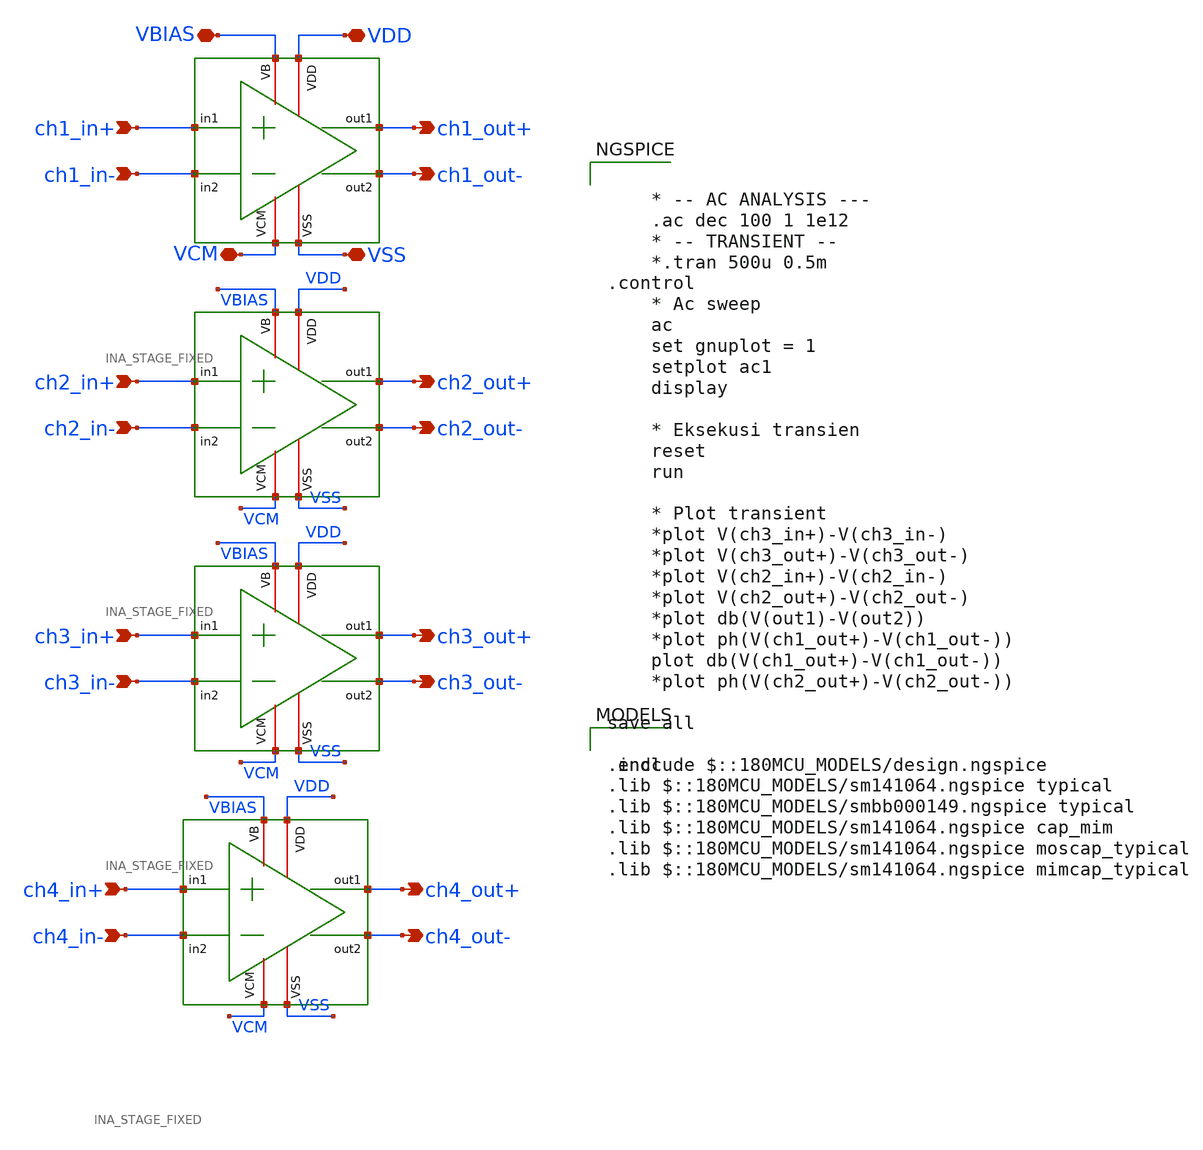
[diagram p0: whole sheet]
** sch_path: ISSCC26/submitted_notebooks/Low Mismatch 4 Channels Instrumentation Amplifier/Instrumentation Amplifier/Schematic and Testbench/FULL_INA_TB.sch
**.subckt FULL_INA_TB ch1_out- ch1_out+ ch1_in+ ch1_in- VCM VBIAS VDD ch2_out- ch2_in+ ch2_in-
*+ ch3_out+ ch3_in+ ch3_in- ch4_out- ch4_out+ ch4_in+ ch4_in- VSS ch3_out- ch2_out+
*.opin ch1_out-
*.opin ch1_out+
*.ipin ch1_in+
*.ipin ch1_in-
*.iopin VCM
*.iopin VBIAS
*.iopin VDD
*.opin ch2_out-
*.ipin ch2_in+
*.ipin ch2_in-
*.opin ch3_out+
*.ipin ch3_in+
*.ipin ch3_in-
*.opin ch4_out-
*.opin ch4_out+
*.ipin ch4_in+
*.ipin ch4_in-
*.iopin VSS
*.opin ch3_out-
*.opin ch2_out+
x1 VCM VDD VBIAS ch1_out- ch1_out+ ch1_in+ ch1_in- VSS INA_STAGE_FIXED
x2 VCM VDD VBIAS ch2_out- ch2_out+ ch2_in+ ch2_in- VSS INA_STAGE_FIXED
x3 VCM VDD VBIAS ch3_out- ch3_out+ ch3_in+ ch3_in- VSS INA_STAGE_FIXED
x4 VCM VDD VBIAS ch4_out- ch4_out+ ch4_in+ ch4_in- VSS INA_STAGE_FIXED
**** begin user architecture code

.include $::180MCU_MODELS/design.ngspice
.lib $::180MCU_MODELS/sm141064.ngspice typical
.lib $::180MCU_MODELS/smbb000149.ngspice typical
.lib $::180MCU_MODELS/sm141064.ngspice cap_mim
.lib $::180MCU_MODELS/sm141064.ngspice moscap_typical
.lib $::180MCU_MODELS/sm141064.ngspice mimcap_typical



	* -- AC ANALYSIS ---
	.ac dec 100 1 1e12
	* -- TRANSIENT --
	*.tran 500u 0.5m
.control
	* Ac sweep
	ac
	set gnuplot = 1
	setplot ac1
	display

	* Eksekusi transien
	reset
	run

	* Plot transient
	*plot V(ch3_in+)-V(ch3_in-)
	*plot V(ch3_out+)-V(ch3_out-)
	*plot V(ch2_in+)-V(ch2_in-)
	*plot V(ch2_out+)-V(ch2_out-)
	*plot db(V(out1)-V(out2))
	*plot ph(V(ch1_out+)-V(ch1_out-))
	plot db(V(ch1_out+)-V(ch1_out-))
	*plot ph(V(ch2_out+)-V(ch2_out-))

save all

.endc


**** end user architecture code
**.ends

* expanding   symbol:  INA_STAGE_FIXED.sym # of pins=8
** sym_path: ISSCC26/submitted_notebooks/Low Mismatch 4 Channels Instrumentation Amplifier/Instrumentation Amplifier/Schematic and Testbench/INA_STAGE_FIXED.sym
** sch_path: ISSCC26/submitted_notebooks/Low Mismatch 4 Channels Instrumentation Amplifier/Instrumentation Amplifier/Schematic and Testbench/INA_STAGE_FIXED.sch
.subckt INA_STAGE_FIXED VCM VDD VB out2 out1 in1 in2 VSS
*.opin out1
*.opin out2
*.ipin in1
*.ipin in2
*.iopin VDD
*.iopin VB
*.iopin VSS
*.iopin VCM
XM10 net1 VB VDD VDD pfet_03v3 L=3u W=0.36u nf=1 ad='int((nf+1)/2) * W/nf * 0.18u' as='int((nf+2)/2) * W/nf * 0.18u'
+ pd='2*int((nf+1)/2) * (W/nf + 0.18u)' ps='2*int((nf+2)/2) * (W/nf + 0.18u)' nrd='0.18u / W' nrs='0.18u / W'
+ sa=0 sb=0 sd=0 m=1
XM11 out1 in1 net1 net1 pfet_03v3 L=3u W=6u nf=6 ad='int((nf+1)/2) * W/nf * 0.18u' as='int((nf+2)/2) * W/nf * 0.18u'
+ pd='2*int((nf+1)/2) * (W/nf + 0.18u)' ps='2*int((nf+2)/2) * (W/nf + 0.18u)' nrd='0.18u / W' nrs='0.18u / W'
+ sa=0 sb=0 sd=0 m=1
XM12 out2 in2 net1 net1 pfet_03v3 L=3u W=6u nf=6 ad='int((nf+1)/2) * W/nf * 0.18u' as='int((nf+2)/2) * W/nf * 0.18u'
+ pd='2*int((nf+1)/2) * (W/nf + 0.18u)' ps='2*int((nf+2)/2) * (W/nf + 0.18u)' nrd='0.18u / W' nrs='0.18u / W'
+ sa=0 sb=0 sd=0 m=1
XM13 out1 in1 net2 net2 nfet_03v3 L=3u W=3u nf=1 ad='int((nf+1)/2) * W/nf * 0.18u' as='int((nf+2)/2) * W/nf * 0.18u'
+ pd='2*int((nf+1)/2) * (W/nf + 0.18u)' ps='2*int((nf+2)/2) * (W/nf + 0.18u)' nrd='0.18u / W' nrs='0.18u / W'
+ sa=0 sb=0 sd=0 m=1
XM14 out2 in2 net2 net2 nfet_03v3 L=3u W=3u nf=1 ad='int((nf+1)/2) * W/nf * 0.18u' as='int((nf+2)/2) * W/nf * 0.18u'
+ pd='2*int((nf+1)/2) * (W/nf + 0.18u)' ps='2*int((nf+2)/2) * (W/nf + 0.18u)' nrd='0.18u / W' nrs='0.18u / W'
+ sa=0 sb=0 sd=0 m=1
XM15 net2 out1 VSS VSS nfet_03v3 L=3u W=0.36u nf=1 ad='int((nf+1)/2) * W/nf * 0.18u' as='int((nf+2)/2) * W/nf * 0.18u'
+ pd='2*int((nf+1)/2) * (W/nf + 0.18u)' ps='2*int((nf+2)/2) * (W/nf + 0.18u)' nrd='0.18u / W' nrs='0.18u / W'
+ sa=0 sb=0 sd=0 m=1
XM16 net2 out2 VSS VSS nfet_03v3 L=3u W=0.36u nf=1 ad='int((nf+1)/2) * W/nf * 0.18u' as='int((nf+2)/2) * W/nf * 0.18u'
+ pd='2*int((nf+1)/2) * (W/nf + 0.18u)' ps='2*int((nf+2)/2) * (W/nf + 0.18u)' nrd='0.18u / W' nrs='0.18u / W'
+ sa=0 sb=0 sd=0 m=1
XM17 VCM VCM in1 in1 pfet_03v3 L=3u W=0.36u nf=1 ad='int((nf+1)/2) * W/nf * 0.18u' as='int((nf+2)/2) * W/nf * 0.18u'
+ pd='2*int((nf+1)/2) * (W/nf + 0.18u)' ps='2*int((nf+2)/2) * (W/nf + 0.18u)' nrd='0.18u / W' nrs='0.18u / W'
+ sa=0 sb=0 sd=0 m=1
XM18 VCM VCM in2 in2 pfet_03v3 L=3u W=0.36u nf=1 ad='int((nf+1)/2) * W/nf * 0.18u' as='int((nf+2)/2) * W/nf * 0.18u'
+ pd='2*int((nf+1)/2) * (W/nf + 0.18u)' ps='2*int((nf+2)/2) * (W/nf + 0.18u)' nrd='0.18u / W' nrs='0.18u / W'
+ sa=0 sb=0 sd=0 m=1
.ends

.end
